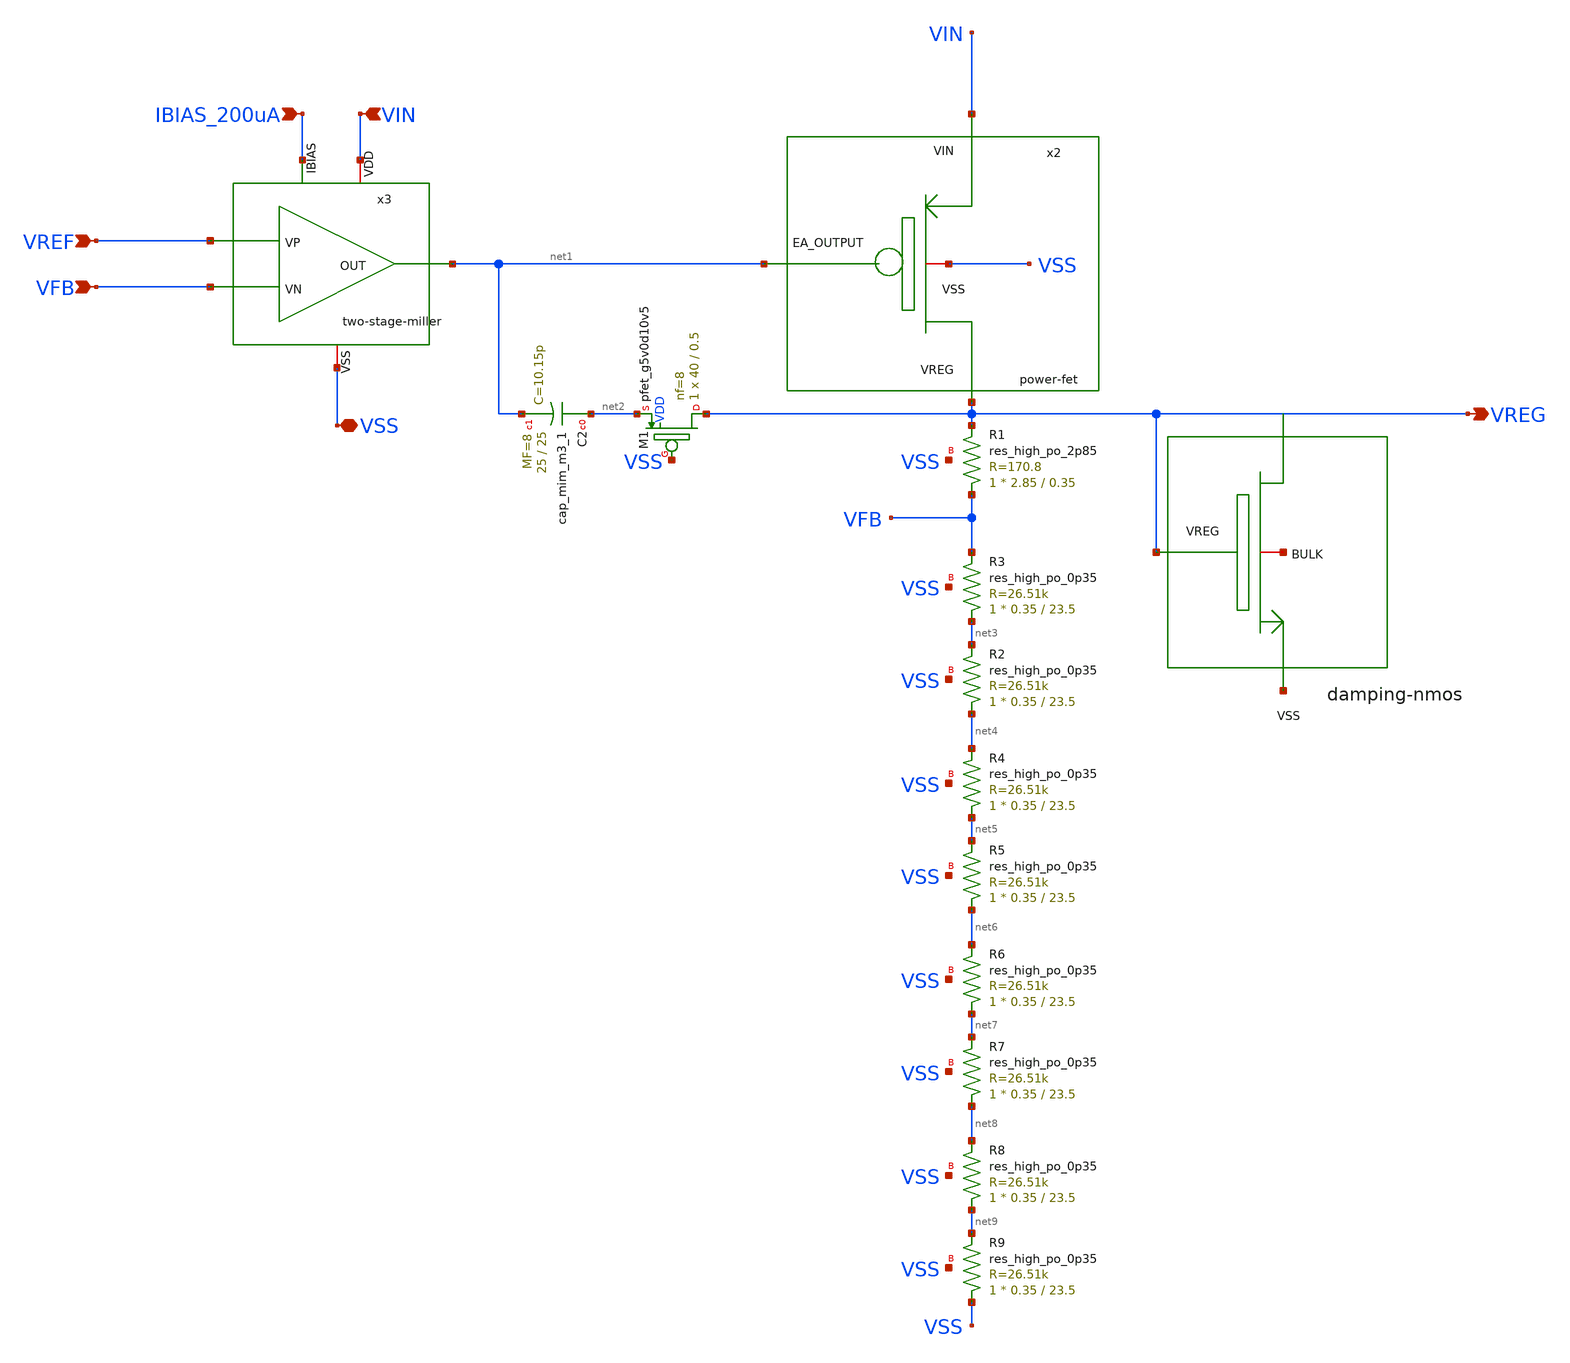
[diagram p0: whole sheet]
** sch_path: xschem/ldo-core/schematics/ldo-top.sch
**.subckt ldo-top VFB VREF IBIAS_200uA VIN VSS VREG
*.ipin VFB
*.ipin VREF
*.ipin IBIAS_200uA
*.ipin VIN
*.iopin VSS
*.opin VREG
x2 VIN VSS net1 VREG power-fet
XR3 net3 VFB VSS sky130_fd_pr__res_high_po_0p35 L=23.5 mult=1 m=1
XR1 VFB VREG VSS sky130_fd_pr__res_high_po_2p85 L=0.35 mult=1 m=1
x3 VIN net1 VREF VFB IBIAS_200uA VSS two-stage-miller
XC2 net2 net1 sky130_fd_pr__cap_mim_m3_1 W=25 L=25 MF=8 m=8
XM1 VREG VSS net2 VDD sky130_fd_pr__pfet_g5v0d10v5 L=0.5 W=40 nf=8 ad='int((nf+1)/2) * W/nf * 0.29' as='int((nf+2)/2) * W/nf * 0.29'
+ pd='2*int((nf+1)/2) * (W/nf + 0.29)' ps='2*int((nf+2)/2) * (W/nf + 0.29)' nrd='0.29 / W' nrs='0.29 / W'
+ sa=0 sb=0 sd=0 mult=1 m=1
XR2 net4 net3 VSS sky130_fd_pr__res_high_po_0p35 L=23.5 mult=1 m=1
XR4 net5 net4 VSS sky130_fd_pr__res_high_po_0p35 L=23.5 mult=1 m=1
XR5 net6 net5 VSS sky130_fd_pr__res_high_po_0p35 L=23.5 mult=1 m=1
XR6 net7 net6 VSS sky130_fd_pr__res_high_po_0p35 L=23.5 mult=1 m=1
XR7 net8 net7 VSS sky130_fd_pr__res_high_po_0p35 L=23.5 mult=1 m=1
XR8 net9 net8 VSS sky130_fd_pr__res_high_po_0p35 L=23.5 mult=1 m=1
XR9 VSS net9 VSS sky130_fd_pr__res_high_po_0p35 L=23.5 mult=1 m=1
x1 VREG net10 net11 damping-nmos
**.ends
.end
